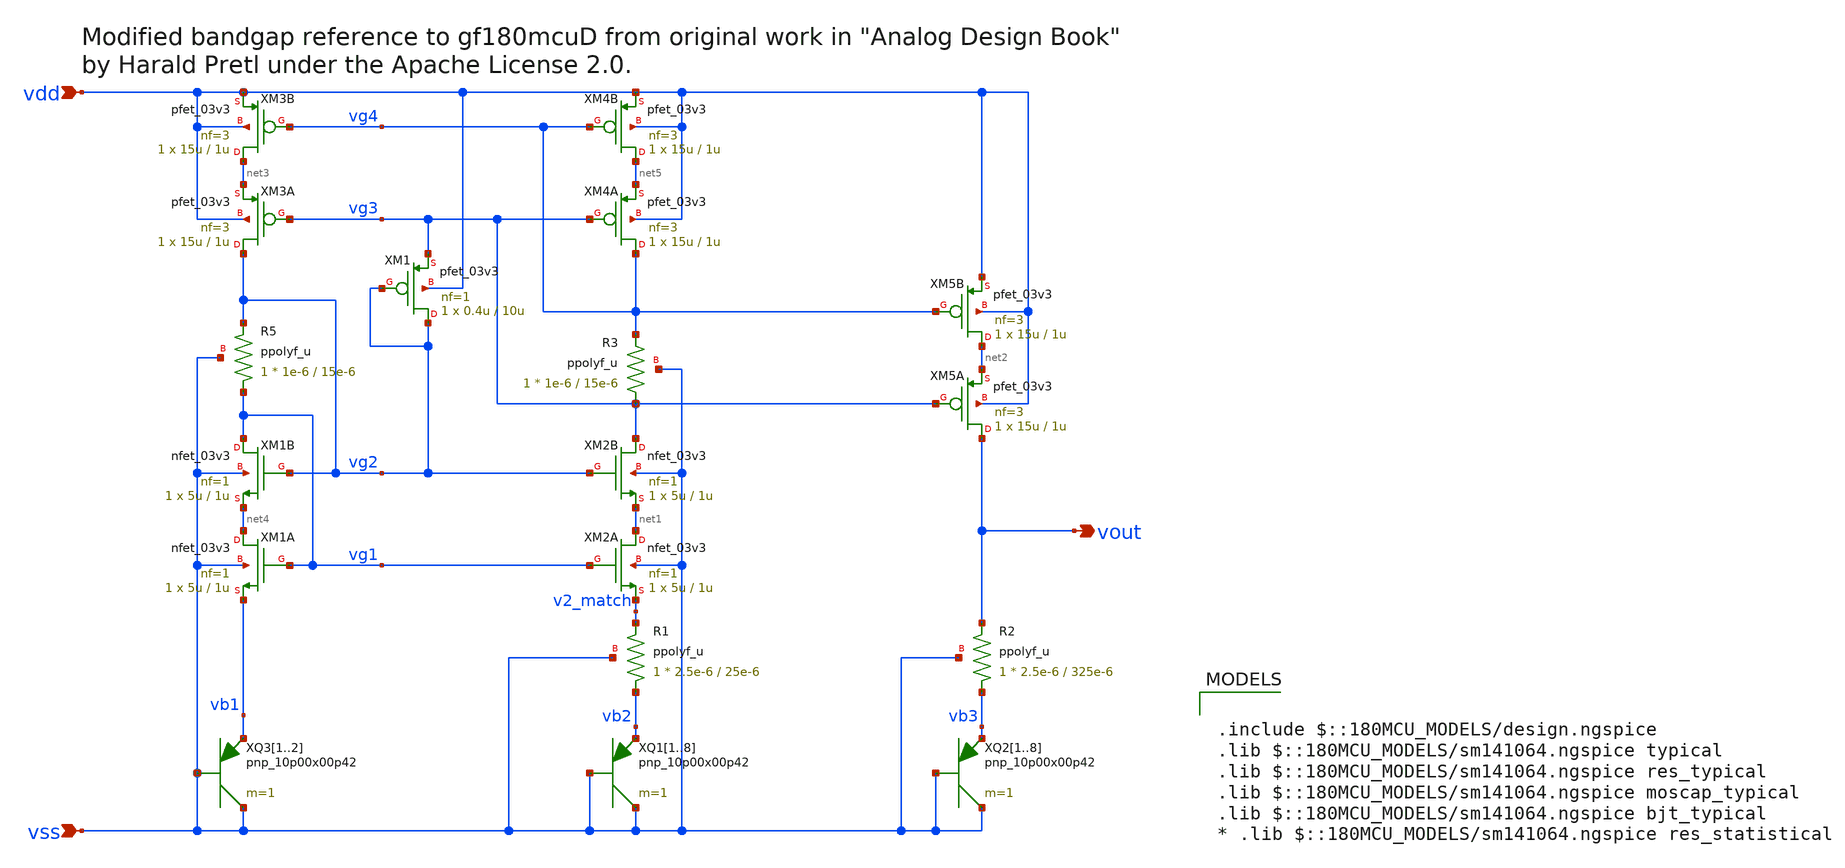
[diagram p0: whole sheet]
** sch_path: designs/libs/core_analog/vref/voltage_reference.sch
* by Harald Pretl under the Apache License 2.0.
**.subckt voltage_reference vdd vout vss
*.ipin vdd
*.opin vout
*.ipin vss
XM1B vg1 vg2 net4 vss nfet_03v3 L=1u W=5u nf=1 ad='int((nf+1)/2) * W/nf * 0.18u' as='int((nf+2)/2) * W/nf * 0.18u'
+ pd='2*int((nf+1)/2) * (W/nf + 0.18u)' ps='2*int((nf+2)/2) * (W/nf + 0.18u)' nrd='0.18u / W' nrs='0.18u / W'
+ sa=0 sb=0 sd=0 m=1
XM1A net4 vg1 vb1 vss nfet_03v3 L=1u W=5u nf=1 ad='int((nf+1)/2) * W/nf * 0.18u' as='int((nf+2)/2) * W/nf * 0.18u'
+ pd='2*int((nf+1)/2) * (W/nf + 0.18u)' ps='2*int((nf+2)/2) * (W/nf + 0.18u)' nrd='0.18u / W' nrs='0.18u / W'
+ sa=0 sb=0 sd=0 m=1
XM2B vg3 vg2 net1 vss nfet_03v3 L=1u W=5u nf=1 ad='int((nf+1)/2) * W/nf * 0.18u' as='int((nf+2)/2) * W/nf * 0.18u'
+ pd='2*int((nf+1)/2) * (W/nf + 0.18u)' ps='2*int((nf+2)/2) * (W/nf + 0.18u)' nrd='0.18u / W' nrs='0.18u / W'
+ sa=0 sb=0 sd=0 m=1
XM2A net1 vg1 v2_match vss nfet_03v3 L=1u W=5u nf=1 ad='int((nf+1)/2) * W/nf * 0.18u' as='int((nf+2)/2) * W/nf * 0.18u'
+ pd='2*int((nf+1)/2) * (W/nf + 0.18u)' ps='2*int((nf+2)/2) * (W/nf + 0.18u)' nrd='0.18u / W' nrs='0.18u / W'
+ sa=0 sb=0 sd=0 m=1
XM4A vg4 vg3 net5 vdd pfet_03v3 L=1u W=15u nf=3 ad='int((nf+1)/2) * W/nf * 0.18u' as='int((nf+2)/2) * W/nf * 0.18u'
+ pd='2*int((nf+1)/2) * (W/nf + 0.18u)' ps='2*int((nf+2)/2) * (W/nf + 0.18u)' nrd='0.18u / W' nrs='0.18u / W'
+ sa=0 sb=0 sd=0 m=1
XM4B net5 vg4 vdd vdd pfet_03v3 L=1u W=15u nf=3 ad='int((nf+1)/2) * W/nf * 0.18u' as='int((nf+2)/2) * W/nf * 0.18u'
+ pd='2*int((nf+1)/2) * (W/nf + 0.18u)' ps='2*int((nf+2)/2) * (W/nf + 0.18u)' nrd='0.18u / W' nrs='0.18u / W'
+ sa=0 sb=0 sd=0 m=1
XM3A vg2 vg3 net3 vdd pfet_03v3 L=1u W=15u nf=3 ad='int((nf+1)/2) * W/nf * 0.18u' as='int((nf+2)/2) * W/nf * 0.18u'
+ pd='2*int((nf+1)/2) * (W/nf + 0.18u)' ps='2*int((nf+2)/2) * (W/nf + 0.18u)' nrd='0.18u / W' nrs='0.18u / W'
+ sa=0 sb=0 sd=0 m=1
XM3B net3 vg4 vdd vdd pfet_03v3 L=1u W=15u nf=3 ad='int((nf+1)/2) * W/nf * 0.18u' as='int((nf+2)/2) * W/nf * 0.18u'
+ pd='2*int((nf+1)/2) * (W/nf + 0.18u)' ps='2*int((nf+2)/2) * (W/nf + 0.18u)' nrd='0.18u / W' nrs='0.18u / W'
+ sa=0 sb=0 sd=0 m=1
XM5A vout vg3 net2 vdd pfet_03v3 L=1u W=15u nf=3 ad='int((nf+1)/2) * W/nf * 0.18u' as='int((nf+2)/2) * W/nf * 0.18u'
+ pd='2*int((nf+1)/2) * (W/nf + 0.18u)' ps='2*int((nf+2)/2) * (W/nf + 0.18u)' nrd='0.18u / W' nrs='0.18u / W'
+ sa=0 sb=0 sd=0 m=1
XM5B net2 vg4 vdd vdd pfet_03v3 L=1u W=15u nf=3 ad='int((nf+1)/2) * W/nf * 0.18u' as='int((nf+2)/2) * W/nf * 0.18u'
+ pd='2*int((nf+1)/2) * (W/nf + 0.18u)' ps='2*int((nf+2)/2) * (W/nf + 0.18u)' nrd='0.18u / W' nrs='0.18u / W'
+ sa=0 sb=0 sd=0 m=1
XQ11 vss vss vb2 pnp_10p00x00p42 m=1 par=1
XQ12 vss vss vb2 pnp_10p00x00p42 m=1 par=1
XQ13 vss vss vb2 pnp_10p00x00p42 m=1 par=1
XQ14 vss vss vb2 pnp_10p00x00p42 m=1 par=1
XQ15 vss vss vb2 pnp_10p00x00p42 m=1 par=1
XQ16 vss vss vb2 pnp_10p00x00p42 m=1 par=1
XQ17 vss vss vb2 pnp_10p00x00p42 m=1 par=1
XQ18 vss vss vb2 pnp_10p00x00p42 m=1 par=1
XQ21 vss vss vb3 pnp_10p00x00p42 m=1 par=1
XQ22 vss vss vb3 pnp_10p00x00p42 m=1 par=1
XQ23 vss vss vb3 pnp_10p00x00p42 m=1 par=1
XQ24 vss vss vb3 pnp_10p00x00p42 m=1 par=1
XQ25 vss vss vb3 pnp_10p00x00p42 m=1 par=1
XQ26 vss vss vb3 pnp_10p00x00p42 m=1 par=1
XQ27 vss vss vb3 pnp_10p00x00p42 m=1 par=1
XQ28 vss vss vb3 pnp_10p00x00p42 m=1 par=1
XQ31 vss vss vb1 pnp_10p00x00p42 m=1 par=1
XQ32 vss vss vb1 pnp_10p00x00p42 m=1 par=1
XM1 vg2 vg2 vg3 vdd pfet_03v3 L=10u W=0.4u nf=1 ad='int((nf+1)/2) * W/nf * 0.18u' as='int((nf+2)/2) * W/nf * 0.18u'
+ pd='2*int((nf+1)/2) * (W/nf + 0.18u)' ps='2*int((nf+2)/2) * (W/nf + 0.18u)' nrd='0.18u / W' nrs='0.18u / W'
+ sa=0 sb=0 sd=0 m=1
XR1 vb2 v2_match vss ppolyf_u r_width=2.5e-6 r_length=25e-6 m=1
XR3 vg3 vg4 vss ppolyf_u r_width=1e-6 r_length=15e-6 m=1
XR5 vg1 vg2 vss ppolyf_u r_width=1e-6 r_length=15e-6 m=1
XR2 vb3 vout vss ppolyf_u r_width=2.5e-6 r_length=325e-6 m=1
**** begin user architecture code

.include $::180MCU_MODELS/design.ngspice
.lib $::180MCU_MODELS/sm141064.ngspice typical
.lib $::180MCU_MODELS/sm141064.ngspice res_typical
.lib $::180MCU_MODELS/sm141064.ngspice moscap_typical
.lib $::180MCU_MODELS/sm141064.ngspice bjt_typical
* .lib $::180MCU_MODELS/sm141064.ngspice res_statistical

**** end user architecture code
**.ends
.end
